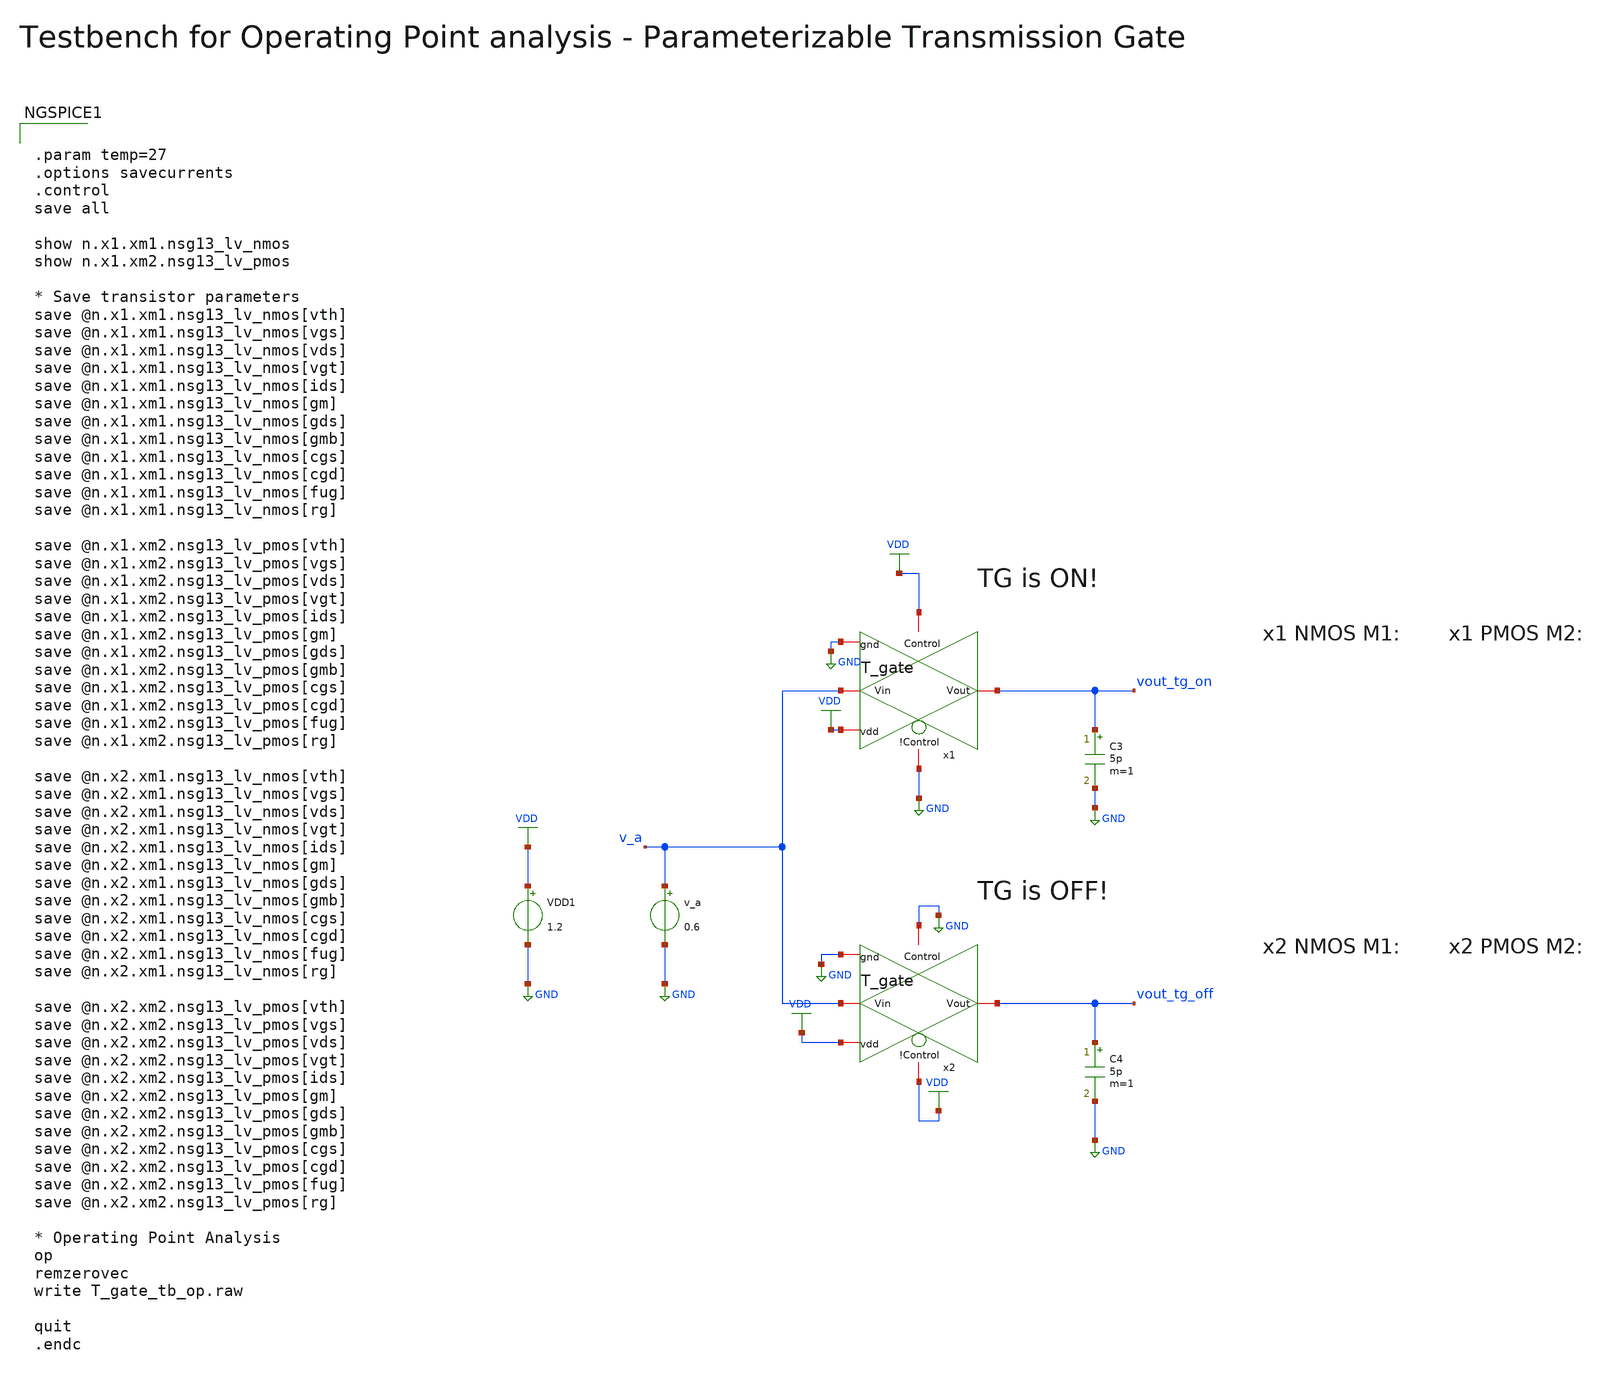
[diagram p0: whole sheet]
** sch_path: xschem/T_gate_tb_op.sch
**.subckt T_gate_tb_op
v_a v_a GND 0.6
VDD1 VDD GND 1.2
C3 vout_tg_on GND 5p m=1
C4 vout_tg_off GND 5p m=1
x1 GND v_a vout_tg_on GND VDD VDD T_gate
x2 VDD v_a vout_tg_off GND GND VDD T_gate
**** begin user architecture code

.lib cornerMOSlv.lib mos_tt
.lib cornerRES.lib res_typ



.param temp=27
.options savecurrents
.control
save all

show n.x1.xm1.nsg13_lv_nmos
show n.x1.xm2.nsg13_lv_pmos

* Save transistor parameters
save @n.x1.xm1.nsg13_lv_nmos[vth]
save @n.x1.xm1.nsg13_lv_nmos[vgs]
save @n.x1.xm1.nsg13_lv_nmos[vds]
save @n.x1.xm1.nsg13_lv_nmos[vgt]
save @n.x1.xm1.nsg13_lv_nmos[ids]
save @n.x1.xm1.nsg13_lv_nmos[gm]
save @n.x1.xm1.nsg13_lv_nmos[gds]
save @n.x1.xm1.nsg13_lv_nmos[gmb]
save @n.x1.xm1.nsg13_lv_nmos[cgs]
save @n.x1.xm1.nsg13_lv_nmos[cgd]
save @n.x1.xm1.nsg13_lv_nmos[fug]
save @n.x1.xm1.nsg13_lv_nmos[rg]

save @n.x1.xm2.nsg13_lv_pmos[vth]
save @n.x1.xm2.nsg13_lv_pmos[vgs]
save @n.x1.xm2.nsg13_lv_pmos[vds]
save @n.x1.xm2.nsg13_lv_pmos[vgt]
save @n.x1.xm2.nsg13_lv_pmos[ids]
save @n.x1.xm2.nsg13_lv_pmos[gm]
save @n.x1.xm2.nsg13_lv_pmos[gds]
save @n.x1.xm2.nsg13_lv_pmos[gmb]
save @n.x1.xm2.nsg13_lv_pmos[cgs]
save @n.x1.xm2.nsg13_lv_pmos[cgd]
save @n.x1.xm2.nsg13_lv_pmos[fug]
save @n.x1.xm2.nsg13_lv_pmos[rg]

save @n.x2.xm1.nsg13_lv_nmos[vth]
save @n.x2.xm1.nsg13_lv_nmos[vgs]
save @n.x2.xm1.nsg13_lv_nmos[vds]
save @n.x2.xm1.nsg13_lv_nmos[vgt]
save @n.x2.xm1.nsg13_lv_nmos[ids]
save @n.x2.xm1.nsg13_lv_nmos[gm]
save @n.x2.xm1.nsg13_lv_nmos[gds]
save @n.x2.xm1.nsg13_lv_nmos[gmb]
save @n.x2.xm1.nsg13_lv_nmos[cgs]
save @n.x2.xm1.nsg13_lv_nmos[cgd]
save @n.x2.xm1.nsg13_lv_nmos[fug]
save @n.x2.xm1.nsg13_lv_nmos[rg]

save @n.x2.xm2.nsg13_lv_pmos[vth]
save @n.x2.xm2.nsg13_lv_pmos[vgs]
save @n.x2.xm2.nsg13_lv_pmos[vds]
save @n.x2.xm2.nsg13_lv_pmos[vgt]
save @n.x2.xm2.nsg13_lv_pmos[ids]
save @n.x2.xm2.nsg13_lv_pmos[gm]
save @n.x2.xm2.nsg13_lv_pmos[gds]
save @n.x2.xm2.nsg13_lv_pmos[gmb]
save @n.x2.xm2.nsg13_lv_pmos[cgs]
save @n.x2.xm2.nsg13_lv_pmos[cgd]
save @n.x2.xm2.nsg13_lv_pmos[fug]
save @n.x2.xm2.nsg13_lv_pmos[rg]

* Operating Point Analysis
op
remzerovec
write T_gate_tb_op.raw

quit
.endc

**** end user architecture code
**.ends

* expanding   symbol:  T_gate.sym # of pins=6
** sym_path: T_gate.sym
** sch_path: T_gate.sch
.subckt T_gate !Control Vin Vout gnd Control vdd
*.iopin Vout
*.iopin Vin
*.iopin !Control
*.iopin Control
*.iopin gnd
*.iopin vdd
XM1 Vin Control Vout gnd sg13_lv_nmos w=1u l=0.13u ng=1 m=1 mm_ok=1
XM2 Vout !Control Vin vdd sg13_lv_pmos w=3u l=0.13u ng=1 m=1 mm_ok=1
.ends

.GLOBAL GND
.GLOBAL VDD
.end
